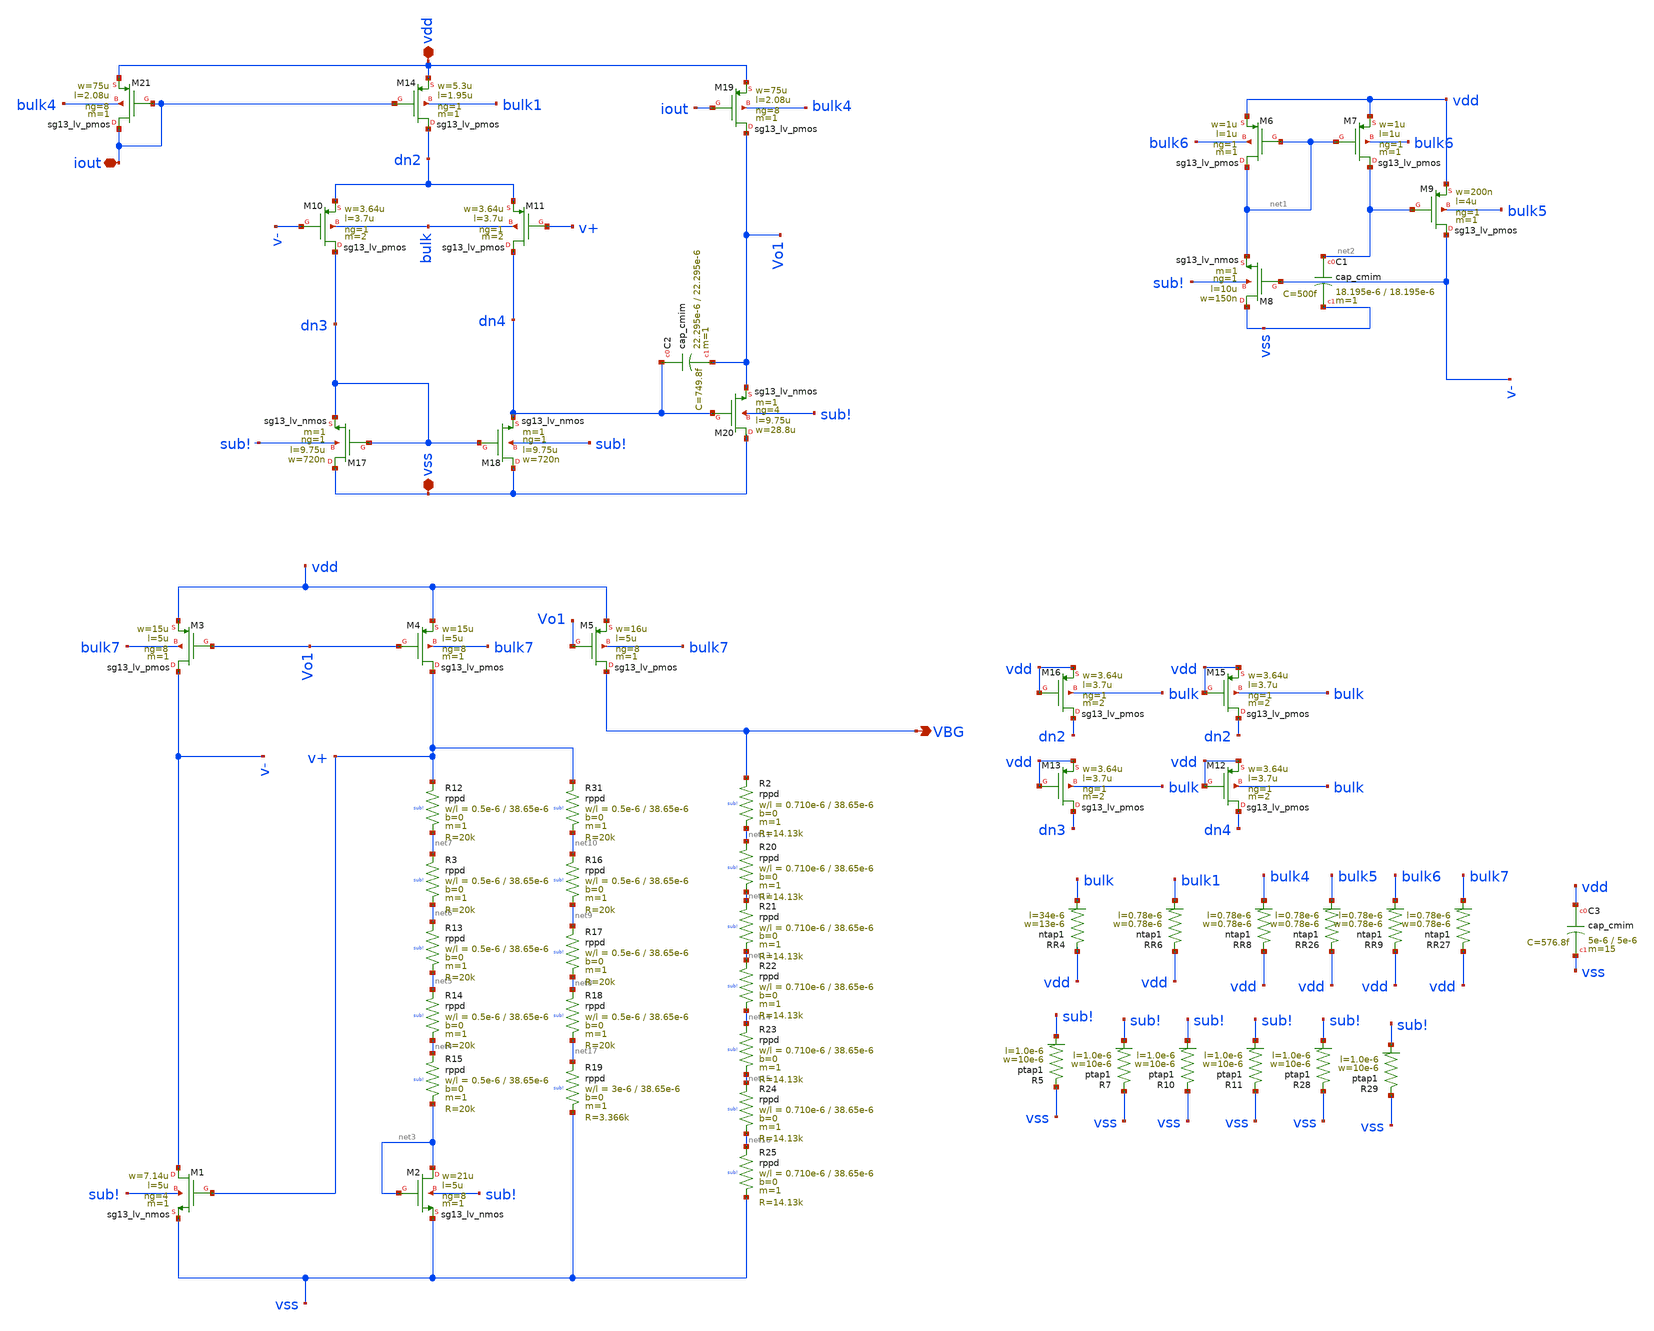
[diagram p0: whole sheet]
** sch_path: schematic/bgr/part_3_layout/BGR_layout/final_bandgapreference/schematic_mod/full_bandgap.sch
**.subckt full_bandgap VBG vss vdd iout
*.opin VBG
*.iopin vss
*.iopin vdd
*.iopin iout
XM8 vss v- net1 sub! sg13_lv_nmos w=150n l=10u ng=1 m=1 mm_ok=1
XM6 net1 net1 vdd bulk6 sg13_lv_pmos w=1u l=1u ng=1 m=1 mm_ok=1
XM7 net2 net1 vdd bulk6 sg13_lv_pmos w=1u l=1u ng=1 m=1 mm_ok=1
XM9 v- net2 vdd bulk5 sg13_lv_pmos w=200n l=4u ng=1 m=1 mm_ok=1
XM1 v- v+ vss sub! sg13_lv_nmos w=7.14u l=5u ng=4 m=1 mm_ok=1
XM2 net3 net3 vss sub! sg13_lv_nmos w=21u l=5u ng=8 m=1 mm_ok=1
XM3 v- Vo1 vdd bulk7 sg13_lv_pmos w=15u l=5u ng=8 m=1 mm_ok=1
XM4 v+ Vo1 vdd bulk7 sg13_lv_pmos w=15u l=5u ng=8 m=1 mm_ok=1
XM5 VBG Vo1 vdd bulk7 sg13_lv_pmos w=16u l=5u ng=8 m=1 mm_ok=1
XR2 VBG net11 sub! rppd w=0.710e-6 l=38.65e-6 m=1 b=0 mm_ok=1
XC1 net2 vss cap_cmim w=18.195e-6 l=18.195e-6 m=1 mm_ok=1
XM10 dn3 v- dn2 bulk sg13_lv_pmos w=3.64u l=3.7u ng=1 m=2 mm_ok=1
XM11 dn4 v+ dn2 bulk sg13_lv_pmos w=3.64u l=3.7u ng=1 m=2 mm_ok=1
XM12 dn4 vdd vdd bulk sg13_lv_pmos w=3.64u l=3.7u ng=1 m=2 mm_ok=1
XM13 dn3 vdd vdd bulk sg13_lv_pmos w=3.64u l=3.7u ng=1 m=2 mm_ok=1
XM15 dn2 vdd vdd bulk sg13_lv_pmos w=3.64u l=3.7u ng=1 m=2 mm_ok=1
XM16 dn2 vdd vdd bulk sg13_lv_pmos w=3.64u l=3.7u ng=1 m=2 mm_ok=1
XR4 vdd bulk ntap1 R=1.828 w=13e-6 l=34e-6
XM14 dn2 iout vdd bulk1 sg13_lv_pmos w=5.3u l=1.95u ng=1 m=1 mm_ok=1
XR5 vss sub! ptap1 R=30.62 w=10e-6 l=1.0e-6
XR6 vdd bulk1 ntap1 R=262.8 w=0.78e-6 l=0.78e-6
XM17 vss dn3 dn3 sub! sg13_lv_nmos w=720n l=9.75u ng=1 m=1 mm_ok=1
XM18 vss dn3 dn4 sub! sg13_lv_nmos w=720n l=9.75u ng=1 m=1 mm_ok=1
XM19 Vo1 iout vdd bulk4 sg13_lv_pmos w=75u l=2.08u ng=8 m=1 mm_ok=1
XM20 vss dn4 Vo1 sub! sg13_lv_nmos w=28.8u l=9.75u ng=4 m=1 mm_ok=1
XM21 iout iout vdd bulk4 sg13_lv_pmos w=75u l=2.08u ng=8 m=1 mm_ok=1
XC2 dn4 Vo1 cap_cmim w=22.295e-6 l=22.295e-6 m=1 mm_ok=1
XR8 vdd bulk4 ntap1 R=262.8 w=0.78e-6 l=0.78e-6
XR9 vdd bulk6 ntap1 R=262.8 w=0.78e-6 l=0.78e-6
XR12 v+ net7 sub! rppd w=0.5e-6 l=38.65e-6 m=1 b=0 mm_ok=1
XR3 net7 net6 sub! rppd w=0.5e-6 l=38.65e-6 m=1 b=0 mm_ok=1
XR13 net6 net5 sub! rppd w=0.5e-6 l=38.65e-6 m=1 b=0 mm_ok=1
XR14 net5 net4 sub! rppd w=0.5e-6 l=38.65e-6 m=1 b=0 mm_ok=1
XR15 net4 net3 sub! rppd w=0.5e-6 l=38.65e-6 m=1 b=0 mm_ok=1
XR16 net10 net9 sub! rppd w=0.5e-6 l=38.65e-6 m=1 b=0 mm_ok=1
XR17 net9 net8 sub! rppd w=0.5e-6 l=38.65e-6 m=1 b=0 mm_ok=1
XR18 net8 net17 sub! rppd w=0.5e-6 l=38.65e-6 m=1 b=0 mm_ok=1
XR19 net17 vss sub! rppd w=3e-6 l=38.65e-6 m=1 b=0 mm_ok=1
XR20 net11 net12 sub! rppd w=0.710e-6 l=38.65e-6 m=1 b=0 mm_ok=1
XR21 net12 net13 sub! rppd w=0.710e-6 l=38.65e-6 m=1 b=0 mm_ok=1
XR22 net13 net14 sub! rppd w=0.710e-6 l=38.65e-6 m=1 b=0 mm_ok=1
XR23 net14 net15 sub! rppd w=0.710e-6 l=38.65e-6 m=1 b=0 mm_ok=1
XR24 net15 net16 sub! rppd w=0.710e-6 l=38.65e-6 m=1 b=0 mm_ok=1
XR25 net16 vss sub! rppd w=0.710e-6 l=38.65e-6 m=1 b=0 mm_ok=1
XR26 vdd bulk5 ntap1 R=262.8 w=0.78e-6 l=0.78e-6
XR27 vdd bulk7 ntap1 R=262.8 w=0.78e-6 l=0.78e-6
XR7 vss sub! ptap1 R=30.62 w=10e-6 l=1.0e-6
XR10 vss sub! ptap1 R=30.62 w=10e-6 l=1.0e-6
XR11 vss sub! ptap1 R=30.62 w=10e-6 l=1.0e-6
XR28 vss sub! ptap1 R=30.62 w=10e-6 l=1.0e-6
XR29 vss sub! ptap1 R=30.62 w=10e-6 l=1.0e-6
XC3 vdd vss cap_cmim w=5e-6 l=5e-6 m=15 mm_ok=1
XR31 v+ net10 sub! rppd w=0.5e-6 l=38.65e-6 m=1 b=0 mm_ok=1
**.ends
.end
